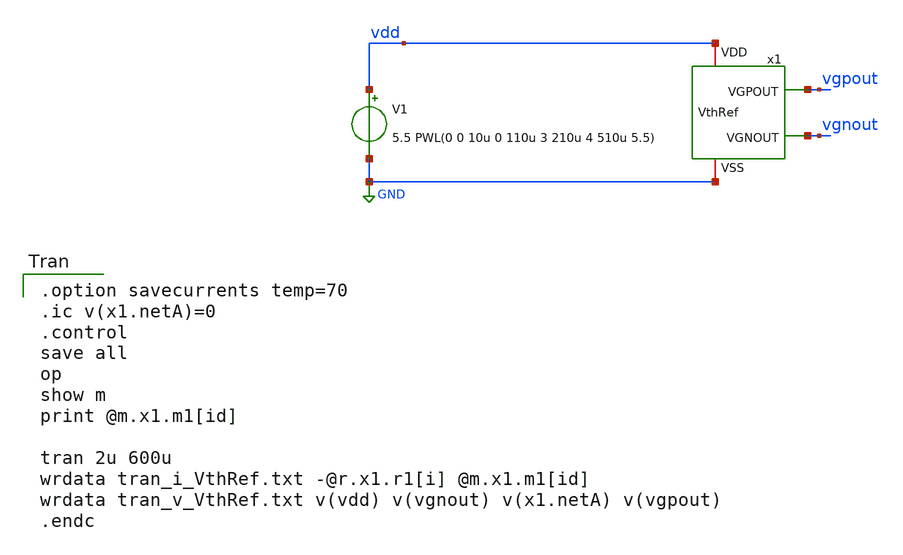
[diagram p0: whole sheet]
** sch_path: member_project/GroupWork/Team_Ando/YuMaehashi/sch/test_VthRef.sch
**.subckt test_VthRef
x1 vdd vgnout GND vgpout VthRef
V1 vdd GND 5.5 PWL(0 0 10u 0 110u 3 210u 4 510u 5.5)
**** begin user architecture code
 .include $::LIB/mos.lib
.include $::LIB/passive.lib
.include $::LIB/diode.lib

.option savecurrents temp=70
.ic v(x1.netA)=0
.control
save all
op
show m
print @m.x1.m1[id]

tran 2u 600u
wrdata tran_i_VthRef.txt -@r.x1.r1[i] @m.x1.m1[id]
wrdata tran_v_VthRef.txt v(vdd) v(vgnout) v(x1.netA) v(vgpout)
.endc

**** end user architecture code
**.ends

* expanding   symbol:  202508_2stageOpAmp/VthRef.sym # of pins=4
** sym_path: member_project/GroupWork/Team_Ando/YuMaehashi/sch/VthRef.sym
** sch_path: member_project/GroupWork/Team_Ando/YuMaehashi/sch/VthRef.sch
.subckt VthRef VDD VGNOUT VSS VGPOUT
*.iopin VDD
*.iopin VSS
*.opin VGNOUT
*.opin VGPOUT
R1 VSS VGNOUT HR_poly W=4 L=24
M1 netA VGNOUT VSS VSS nmos L=4u W=2u m=2
M2 VGPOUT netA VGNOUT VSS nmos L=2u W=10u m=8
M3 netA VGPOUT VDD VDD pmos L=2.5u W=10u m=10
M4 VGPOUT VGPOUT VDD VDD pmos L=2.5u W=10u m=10
M5 netB netB VSS VSS nmos L=10u W=2u m=1
M6 VDD netB netA VSS nmos L=4u W=2u m=2
M7 net1 VSS VDD VDD pmos L=10u W=2u m=1
M8 netB netB net1 VDD pmos L=10u W=2u m=1
R3 VSS VSS HR_poly W=44 L=24
M9 VSS VSS VSS VSS nmos L=2u W=2u m=1
M10 VSS VSS VGNOUT VSS nmos L=2u W=10u m=2
M11 VDD VDD VDD VDD pmos L=2.5u W=10u m=2
.ends

.GLOBAL GND
.end
